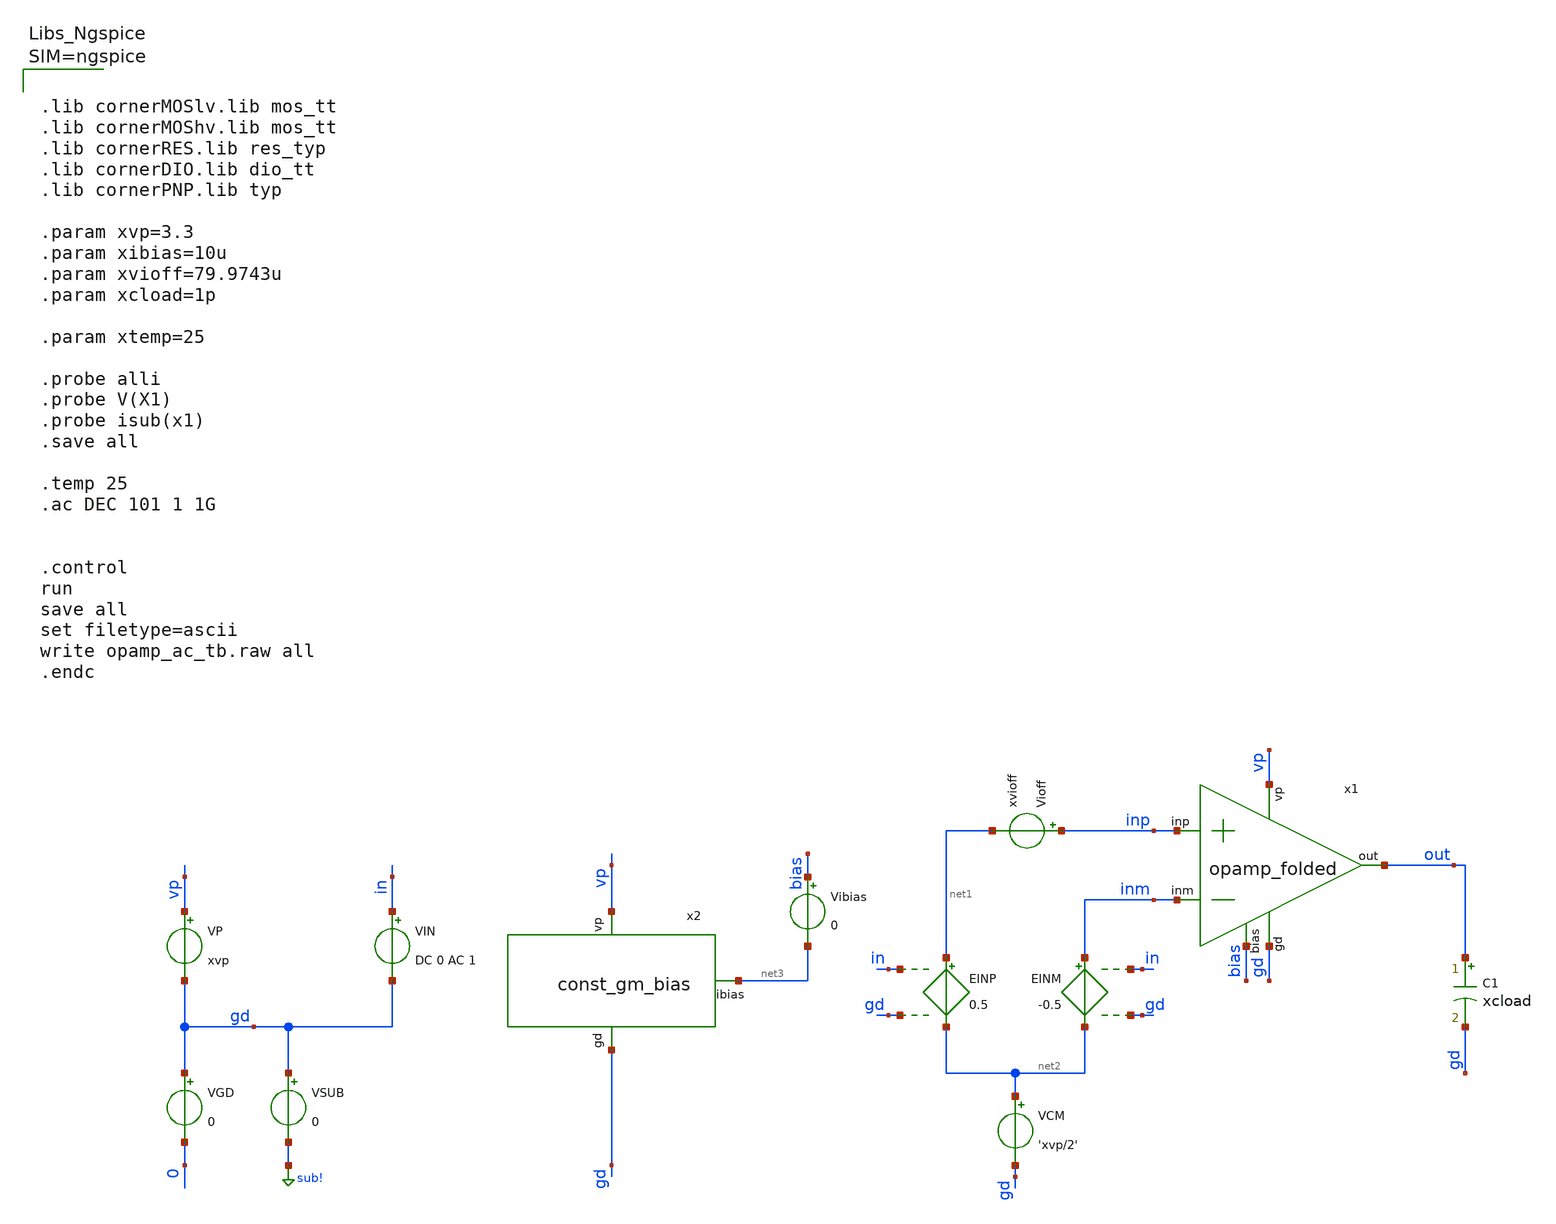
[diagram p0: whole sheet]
** sch_path: PLL0663-main/testbenches/ac/xschem/bandgap/opamp_ac_tb.sch
**.subckt opamp_ac_tb
EINP net1 net2 in gd 0.5
EINM inm net2 in gd -0.5
C1 out gd xcload m=1
VGD gd 0 0
VP vp gd xvp
VSUB gd sub! 0
VIN in gd DC 0 AC 1
VCM net2 gd 'xvp/2'
Vibias bias net3 0
.save i(vibias)
Vioff inp net1 xvioff
x1 vp inp inm out bias gd opamp_folded
x2 vp net3 gd const_gm_bias
**** begin user architecture code



.lib cornerMOSlv.lib mos_tt
.lib cornerMOShv.lib mos_tt
.lib cornerRES.lib res_typ
.lib cornerDIO.lib dio_tt
.lib cornerPNP.lib typ

.param xvp=3.3
.param xibias=10u
.param xvioff=79.9743u
.param xcload=1p

.param xtemp=25

.probe alli
.probe V(X1)
.probe isub(x1)
.save all

.temp 25
.ac DEC 101 1 1G


.control
run
save all
set filetype=ascii
write opamp_ac_tb.raw all
.endc



**** end user architecture code
**.ends
.GLOBAL sub!
.end
